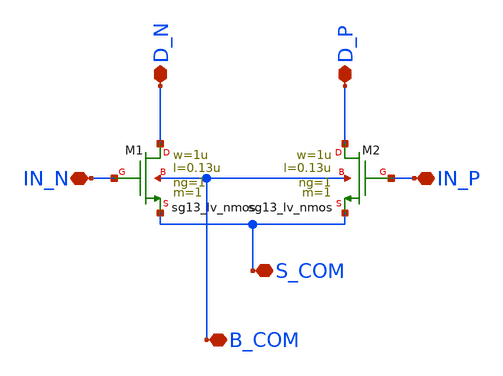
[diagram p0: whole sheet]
** sch_path: xschem/Proyecto/klayout/diff_pair.sch
**.subckt diff_pair D_N D_P S_COM IN_P B_COM IN_N
*.iopin D_N
*.iopin D_P
*.iopin S_COM
*.iopin IN_P
*.iopin B_COM
*.iopin IN_N
XM1 D_N IN_N S_COM B_COM sg13_lv_nmos w=1u l=0.13u ng=1 m=1 mm_ok=1
XM2 D_P IN_P S_COM B_COM sg13_lv_nmos w=1u l=0.13u ng=1 m=1 mm_ok=1
**.ends
.end
